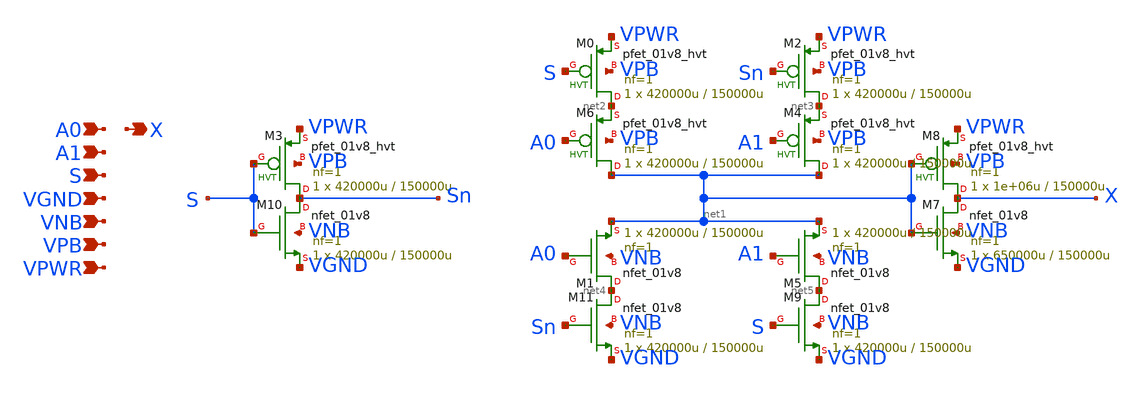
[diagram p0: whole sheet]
** sch_path: schematics/mux2/sky130_fd_sc_hd__mux2_1.sch
**.subckt sky130_fd_sc_hd__mux2_1 A0 A1 S VGND VNB VPB VPWR X
*.ipin A0
*.ipin A1
*.ipin S
*.ipin VGND
*.ipin VNB
*.ipin VPB
*.ipin VPWR
*.opin X
XM8 X net1 VPWR VPB sky130_fd_pr__pfet_01v8_hvt L=150000u W=1e+06u nf=1 ad='int((1 + 1)/2) * 1e+06u / 1 * 0.29'
+ as='int((1 + 2)/2) * 1e+06u / 1 * 0.29' pd='2*int((1 + 1)/2) * (1e+06u / 1 + 0.29)' ps='2*int((1 + 2)/2) * (1e+06u / 1 + 0.29)'
+ nrd='0.29 / 1e+06u ' nrs='0.29 / 1e+06u ' sa=0 sb=0 sd=0 mult=1 m=1
XM7 X net1 VGND VNB sky130_fd_pr__nfet_01v8 L=150000u W=650000u nf=1 ad='int((1 + 1)/2) * 650000u / 1 * 0.29'
+ as='int((1 + 2)/2) * 650000u / 1 * 0.29' pd='2*int((1 + 1)/2) * (650000u / 1 + 0.29)' ps='2*int((1 + 2)/2) * (650000u / 1 + 0.29)'
+ nrd='0.29 / 650000u ' nrs='0.29 / 650000u ' sa=0 sb=0 sd=0 mult=1 m=1
XM3 Sn S VPWR VPB sky130_fd_pr__pfet_01v8_hvt L=150000u W=420000u nf=1 ad='int((1 + 1)/2) * 420000u / 1 * 0.29'
+ as='int((1 + 2)/2) * 420000u / 1 * 0.29' pd='2*int((1 + 1)/2) * (420000u / 1 + 0.29)' ps='2*int((1 + 2)/2) * (420000u / 1 + 0.29)'
+ nrd='0.29 / 420000u ' nrs='0.29 / 420000u ' sa=0 sb=0 sd=0 mult=1 m=1
XM10 Sn S VGND VNB sky130_fd_pr__nfet_01v8 L=150000u W=420000u nf=1 ad='int((1 + 1)/2) * 420000u / 1 * 0.29'
+ as='int((1 + 2)/2) * 420000u / 1 * 0.29' pd='2*int((1 + 1)/2) * (420000u / 1 + 0.29)' ps='2*int((1 + 2)/2) * (420000u / 1 + 0.29)'
+ nrd='0.29 / 420000u ' nrs='0.29 / 420000u ' sa=0 sb=0 sd=0 mult=1 m=1
XM6 net1 A0 net2 VPB sky130_fd_pr__pfet_01v8_hvt L=150000u W=420000u nf=1 ad='int((1 + 1)/2) * 420000u / 1 * 0.29'
+ as='int((1 + 2)/2) * 420000u / 1 * 0.29' pd='2*int((1 + 1)/2) * (420000u / 1 + 0.29)' ps='2*int((1 + 2)/2) * (420000u / 1 + 0.29)'
+ nrd='0.29 / 420000u ' nrs='0.29 / 420000u ' sa=0 sb=0 sd=0 mult=1 m=1
XM4 net1 A1 net3 VPB sky130_fd_pr__pfet_01v8_hvt L=150000u W=420000u nf=1 ad='int((1 + 1)/2) * 420000u / 1 * 0.29'
+ as='int((1 + 2)/2) * 420000u / 1 * 0.29' pd='2*int((1 + 1)/2) * (420000u / 1 + 0.29)' ps='2*int((1 + 2)/2) * (420000u / 1 + 0.29)'
+ nrd='0.29 / 420000u ' nrs='0.29 / 420000u ' sa=0 sb=0 sd=0 mult=1 m=1
XM2 net3 Sn VPWR VPB sky130_fd_pr__pfet_01v8_hvt L=150000u W=420000u nf=1 ad='int((1 + 1)/2) * 420000u / 1 * 0.29'
+ as='int((1 + 2)/2) * 420000u / 1 * 0.29' pd='2*int((1 + 1)/2) * (420000u / 1 + 0.29)' ps='2*int((1 + 2)/2) * (420000u / 1 + 0.29)'
+ nrd='0.29 / 420000u ' nrs='0.29 / 420000u ' sa=0 sb=0 sd=0 mult=1 m=1
XM0 net2 S VPWR VPB sky130_fd_pr__pfet_01v8_hvt L=150000u W=420000u nf=1 ad='int((1 + 1)/2) * 420000u / 1 * 0.29'
+ as='int((1 + 2)/2) * 420000u / 1 * 0.29' pd='2*int((1 + 1)/2) * (420000u / 1 + 0.29)' ps='2*int((1 + 2)/2) * (420000u / 1 + 0.29)'
+ nrd='0.29 / 420000u ' nrs='0.29 / 420000u ' sa=0 sb=0 sd=0 mult=1 m=1
XM1 net4 A0 net1 VNB sky130_fd_pr__nfet_01v8 L=150000u W=420000u nf=1 ad='int((1 + 1)/2) * 420000u / 1 * 0.29'
+ as='int((1 + 2)/2) * 420000u / 1 * 0.29' pd='2*int((1 + 1)/2) * (420000u / 1 + 0.29)' ps='2*int((1 + 2)/2) * (420000u / 1 + 0.29)'
+ nrd='0.29 / 420000u ' nrs='0.29 / 420000u ' sa=0 sb=0 sd=0 mult=1 m=1
XM5 net5 A1 net1 VNB sky130_fd_pr__nfet_01v8 L=150000u W=420000u nf=1 ad='int((1 + 1)/2) * 420000u / 1 * 0.29'
+ as='int((1 + 2)/2) * 420000u / 1 * 0.29' pd='2*int((1 + 1)/2) * (420000u / 1 + 0.29)' ps='2*int((1 + 2)/2) * (420000u / 1 + 0.29)'
+ nrd='0.29 / 420000u ' nrs='0.29 / 420000u ' sa=0 sb=0 sd=0 mult=1 m=1
XM11 net4 Sn VGND VNB sky130_fd_pr__nfet_01v8 L=150000u W=420000u nf=1 ad='int((1 + 1)/2) * 420000u / 1 * 0.29'
+ as='int((1 + 2)/2) * 420000u / 1 * 0.29' pd='2*int((1 + 1)/2) * (420000u / 1 + 0.29)' ps='2*int((1 + 2)/2) * (420000u / 1 + 0.29)'
+ nrd='0.29 / 420000u ' nrs='0.29 / 420000u ' sa=0 sb=0 sd=0 mult=1 m=1
XM9 net5 S VGND VNB sky130_fd_pr__nfet_01v8 L=150000u W=420000u nf=1 ad='int((1 + 1)/2) * 420000u / 1 * 0.29'
+ as='int((1 + 2)/2) * 420000u / 1 * 0.29' pd='2*int((1 + 1)/2) * (420000u / 1 + 0.29)' ps='2*int((1 + 2)/2) * (420000u / 1 + 0.29)'
+ nrd='0.29 / 420000u ' nrs='0.29 / 420000u ' sa=0 sb=0 sd=0 mult=1 m=1
**.ends
.end
